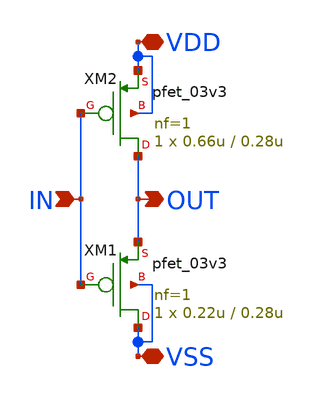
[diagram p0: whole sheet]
** sch_path: w1_advanced-foundation/w1_task/w1_inv-ring/untitled.sch
**.subckt untitled VDD VSS IN OUT
*.iopin VDD
*.iopin VSS
*.ipin IN
*.opin OUT
XM1 VSS IN OUT VSS pfet_03v3 L=0.28u W=0.22u nf=1 ad='int((nf+1)/2) * W/nf * 0.18u' as='int((nf+2)/2) * W/nf * 0.18u'
+ pd='2*int((nf+1)/2) * (W/nf + 0.18u)' ps='2*int((nf+2)/2) * (W/nf + 0.18u)' nrd='0.18u / W' nrs='0.18u / W'
+ sa=0 sb=0 sd=0 m=1
XM2 OUT IN VDD VDD pfet_03v3 L=0.28u W=0.66u nf=1 ad='int((nf+1)/2) * W/nf * 0.18u' as='int((nf+2)/2) * W/nf * 0.18u'
+ pd='2*int((nf+1)/2) * (W/nf + 0.18u)' ps='2*int((nf+2)/2) * (W/nf + 0.18u)' nrd='0.18u / W' nrs='0.18u / W'
+ sa=0 sb=0 sd=0 m=1
**.ends
.end
